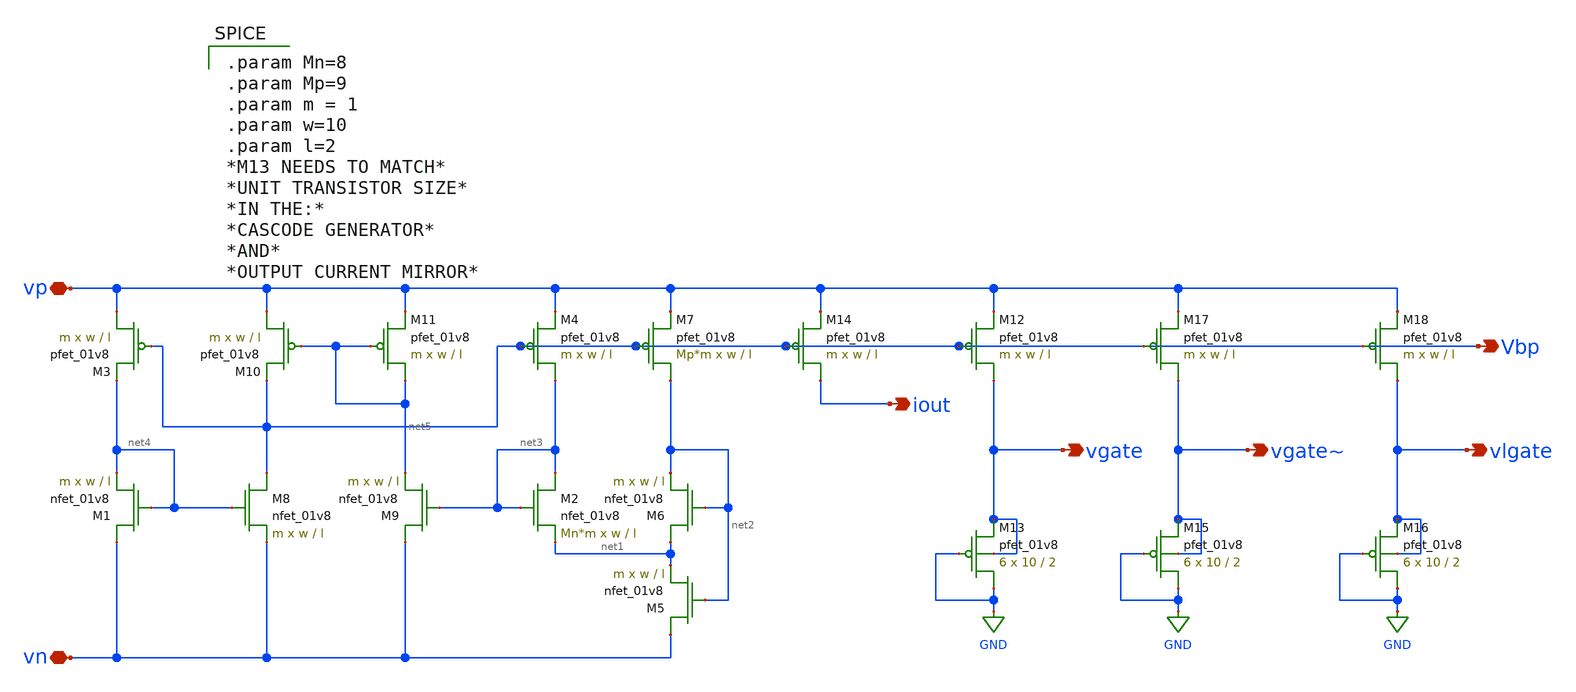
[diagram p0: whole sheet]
** sch_path: schematic/old/bias_current.sch
**.subckt bias_current vp vn iout Vbp vgate vgate~ vlgate
*.iopin vp
*.iopin vn
*.opin iout
*.opin Vbp
*.opin vgate
*.opin vgate~
*.opin vlgate
XM1 vn net4 net4 GND sky130_fd_pr__nfet_01v8 L=l W=w nf=1 ad='int((nf+1)/2) * W/nf * 0.29' as='int((nf+2)/2) * W/nf * 0.29'
+ pd='2*int((nf+1)/2) * (W/nf + 0.29)' ps='2*int((nf+2)/2) * (W/nf + 0.29)' nrd='0.29 / W' nrs='0.29 / W'
+ sa=0 sb=0 sd=0 mult=m m=m
XM2 net3 net3 net1 GND sky130_fd_pr__nfet_01v8 L=l W=w nf=1 ad='int((nf+1)/2) * W/nf * 0.29' as='int((nf+2)/2) * W/nf * 0.29'
+ pd='2*int((nf+1)/2) * (W/nf + 0.29)' ps='2*int((nf+2)/2) * (W/nf + 0.29)' nrd='0.29 / W' nrs='0.29 / W'
+ sa=0 sb=0 sd=0 mult=Mn*m m=Mn*m
XM3 vp Vbp net4 VDD sky130_fd_pr__pfet_01v8 L=l W=w nf=1 ad='int((nf+1)/2) * W/nf * 0.29' as='int((nf+2)/2) * W/nf * 0.29'
+ pd='2*int((nf+1)/2) * (W/nf + 0.29)' ps='2*int((nf+2)/2) * (W/nf + 0.29)' nrd='0.29 / W' nrs='0.29 / W'
+ sa=0 sb=0 sd=0 mult=m m=m
XM4 net3 Vbp vp VDD sky130_fd_pr__pfet_01v8 L=l W=w nf=1 ad='int((nf+1)/2) * W/nf * 0.29' as='int((nf+2)/2) * W/nf * 0.29'
+ pd='2*int((nf+1)/2) * (W/nf + 0.29)' ps='2*int((nf+2)/2) * (W/nf + 0.29)' nrd='0.29 / W' nrs='0.29 / W'
+ sa=0 sb=0 sd=0 mult=m m=m
XM5 vn net2 net1 GND sky130_fd_pr__nfet_01v8 L=l W=w nf=1 ad='int((nf+1)/2) * W/nf * 0.29' as='int((nf+2)/2) * W/nf * 0.29'
+ pd='2*int((nf+1)/2) * (W/nf + 0.29)' ps='2*int((nf+2)/2) * (W/nf + 0.29)' nrd='0.29 / W' nrs='0.29 / W'
+ sa=0 sb=0 sd=0 mult=m m=m
XM6 net1 net2 net2 GND sky130_fd_pr__nfet_01v8 L=l W=w nf=1 ad='int((nf+1)/2) * W/nf * 0.29' as='int((nf+2)/2) * W/nf * 0.29'
+ pd='2*int((nf+1)/2) * (W/nf + 0.29)' ps='2*int((nf+2)/2) * (W/nf + 0.29)' nrd='0.29 / W' nrs='0.29 / W'
+ sa=0 sb=0 sd=0 mult=m m=m
XM7 net2 Vbp vp VDD sky130_fd_pr__pfet_01v8 L=l W=w nf=1 ad='int((nf+1)/2) * W/nf * 0.29' as='int((nf+2)/2) * W/nf * 0.29'
+ pd='2*int((nf+1)/2) * (W/nf + 0.29)' ps='2*int((nf+2)/2) * (W/nf + 0.29)' nrd='0.29 / W' nrs='0.29 / W'
+ sa=0 sb=0 sd=0 mult=Mp*m m=Mp*m
XM8 Vbp net4 vn GND sky130_fd_pr__nfet_01v8 L=l W=w nf=1 ad='int((nf+1)/2) * W/nf * 0.29' as='int((nf+2)/2) * W/nf * 0.29'
+ pd='2*int((nf+1)/2) * (W/nf + 0.29)' ps='2*int((nf+2)/2) * (W/nf + 0.29)' nrd='0.29 / W' nrs='0.29 / W'
+ sa=0 sb=0 sd=0 mult=m m=m
XM9 vn net3 net5 GND sky130_fd_pr__nfet_01v8 L=l W=w nf=1 ad='int((nf+1)/2) * W/nf * 0.29' as='int((nf+2)/2) * W/nf * 0.29'
+ pd='2*int((nf+1)/2) * (W/nf + 0.29)' ps='2*int((nf+2)/2) * (W/nf + 0.29)' nrd='0.29 / W' nrs='0.29 / W'
+ sa=0 sb=0 sd=0 mult=m m=m
XM10 vp net5 Vbp VDD sky130_fd_pr__pfet_01v8 L=l W=w nf=1 ad='int((nf+1)/2) * W/nf * 0.29' as='int((nf+2)/2) * W/nf * 0.29'
+ pd='2*int((nf+1)/2) * (W/nf + 0.29)' ps='2*int((nf+2)/2) * (W/nf + 0.29)' nrd='0.29 / W' nrs='0.29 / W'
+ sa=0 sb=0 sd=0 mult=m m=m
XM11 net5 net5 vp VDD sky130_fd_pr__pfet_01v8 L=l W=w nf=1 ad='int((nf+1)/2) * W/nf * 0.29' as='int((nf+2)/2) * W/nf * 0.29'
+ pd='2*int((nf+1)/2) * (W/nf + 0.29)' ps='2*int((nf+2)/2) * (W/nf + 0.29)' nrd='0.29 / W' nrs='0.29 / W'
+ sa=0 sb=0 sd=0 mult=m m=m
XM14 iout Vbp vp VDD sky130_fd_pr__pfet_01v8 L=l W=w nf=1 ad='int((nf+1)/2) * W/nf * 0.29' as='int((nf+2)/2) * W/nf * 0.29'
+ pd='2*int((nf+1)/2) * (W/nf + 0.29)' ps='2*int((nf+2)/2) * (W/nf + 0.29)' nrd='0.29 / W' nrs='0.29 / W'
+ sa=0 sb=0 sd=0 mult=m m=m
XM12 vgate Vbp vp VDD sky130_fd_pr__pfet_01v8 L=l W=w nf=1 ad='int((nf+1)/2) * W/nf * 0.29' as='int((nf+2)/2) * W/nf * 0.29'
+ pd='2*int((nf+1)/2) * (W/nf + 0.29)' ps='2*int((nf+2)/2) * (W/nf + 0.29)' nrd='0.29 / W' nrs='0.29 / W'
+ sa=0 sb=0 sd=0 mult=m m=m
XM13 GND GND vgate vgate sky130_fd_pr__pfet_01v8 L=2 W=10 nf=1 ad='int((nf+1)/2) * W/nf * 0.29' as='int((nf+2)/2) * W/nf * 0.29'
+ pd='2*int((nf+1)/2) * (W/nf + 0.29)' ps='2*int((nf+2)/2) * (W/nf + 0.29)' nrd='0.29 / W' nrs='0.29 / W'
+ sa=0 sb=0 sd=0 mult=6 m=6
XM15 GND GND vgate~ vgate~ sky130_fd_pr__pfet_01v8 L=2 W=10 nf=1 ad='int((nf+1)/2) * W/nf * 0.29' as='int((nf+2)/2) * W/nf * 0.29'
+ pd='2*int((nf+1)/2) * (W/nf + 0.29)' ps='2*int((nf+2)/2) * (W/nf + 0.29)' nrd='0.29 / W' nrs='0.29 / W'
+ sa=0 sb=0 sd=0 mult=6 m=6
XM16 GND GND vlgate vlgate sky130_fd_pr__pfet_01v8 L=2 W=10 nf=1 ad='int((nf+1)/2) * W/nf * 0.29' as='int((nf+2)/2) * W/nf * 0.29'
+ pd='2*int((nf+1)/2) * (W/nf + 0.29)' ps='2*int((nf+2)/2) * (W/nf + 0.29)' nrd='0.29 / W' nrs='0.29 / W'
+ sa=0 sb=0 sd=0 mult=6 m=6
XM17 vgate~ Vbp vp VDD sky130_fd_pr__pfet_01v8 L=l W=w nf=1 ad='int((nf+1)/2) * W/nf * 0.29' as='int((nf+2)/2) * W/nf * 0.29'
+ pd='2*int((nf+1)/2) * (W/nf + 0.29)' ps='2*int((nf+2)/2) * (W/nf + 0.29)' nrd='0.29 / W' nrs='0.29 / W'
+ sa=0 sb=0 sd=0 mult=m m=m
XM18 vlgate Vbp vp VDD sky130_fd_pr__pfet_01v8 L=l W=w nf=1 ad='int((nf+1)/2) * W/nf * 0.29' as='int((nf+2)/2) * W/nf * 0.29'
+ pd='2*int((nf+1)/2) * (W/nf + 0.29)' ps='2*int((nf+2)/2) * (W/nf + 0.29)' nrd='0.29 / W' nrs='0.29 / W'
+ sa=0 sb=0 sd=0 mult=m m=m
**** begin user architecture code

.param Mn=8
.param Mp=9
.param m = 1
.param w=10
.param l=2
*M13 NEEDS TO MATCH*
*UNIT TRANSISTOR SIZE*
*IN THE:*
*CASCODE GENERATOR*
*AND*
*OUTPUT CURRENT MIRROR*

**** end user architecture code
**.ends
.GLOBAL GND
.end
